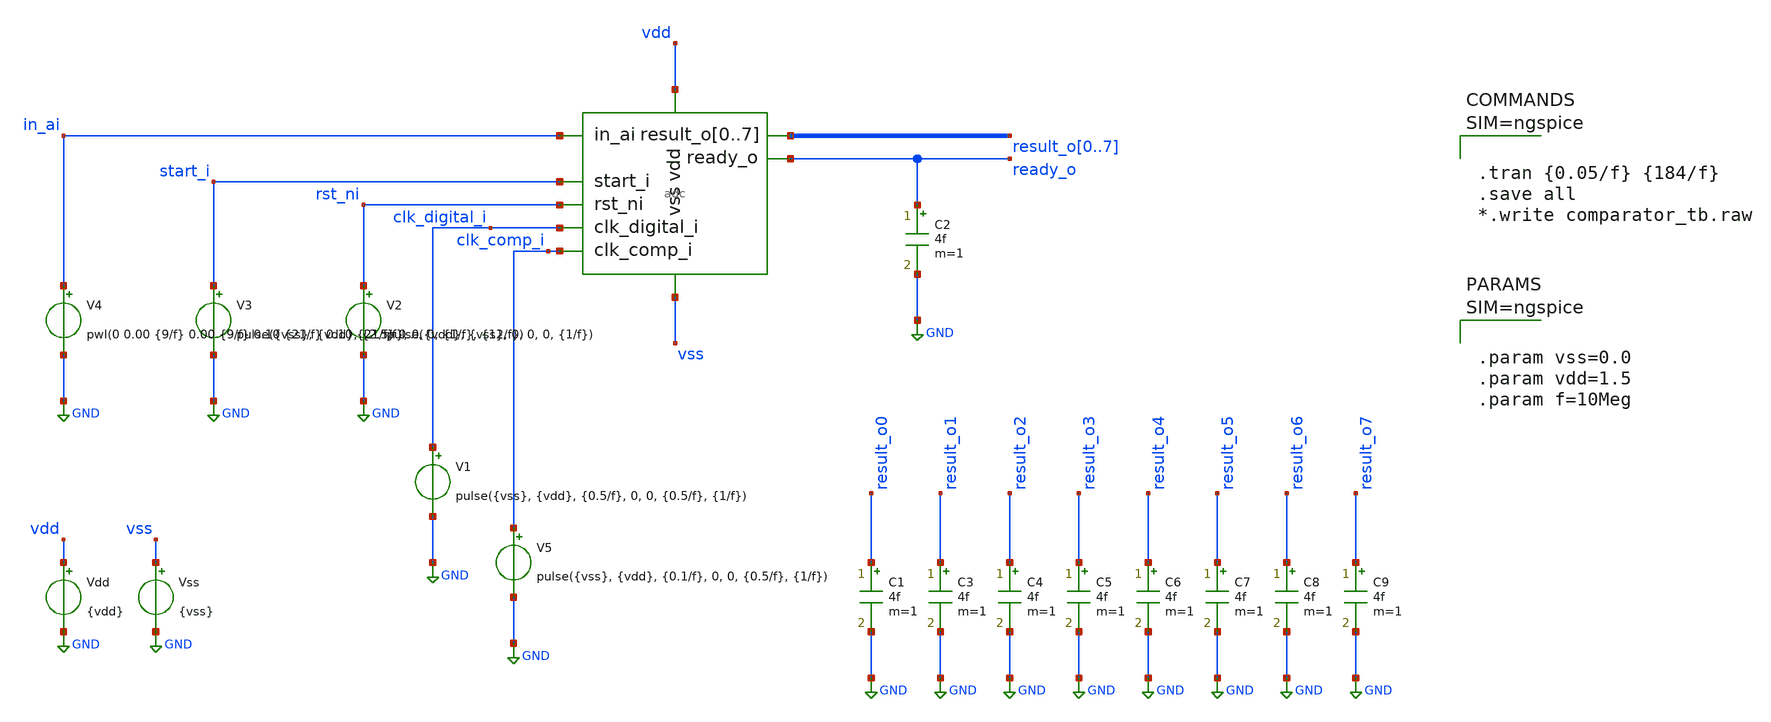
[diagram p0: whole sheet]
** sch_path: designs/basic1/adc_tb.sch
* IHP-GmbH/IHP-Open-PDK/ihp-sg13g2/libs.tech/xschem/sg13g2_stdcells/sg13g2_inv_2.sch:
* Copyright 2023 IHP PDK Authors
* Licensed under the Apache License, Version 2.0 (the "License");
**.subckt adc_tb
x1 in_ai start_i rst_ni clk_digital_i result_o0 result_o1 result_o2 result_o3 result_o4 result_o5
+ result_o6 result_o7 ready_o vdd vss clk_comp_i adc
V1 clk_digital_i GND pulse({vss}, {vdd}, {0.5/f}, 0, 0, {0.5/f}, {1/f})
V2 rst_ni GND pulse({vdd}, {vss}, 0, 0, 0, {1/f})
V3 start_i GND pulse({vss}, {vdd}, {2.5/f}, 0, 0, {1/f}, {12/f})
V4 in_ai GND pwl(0 0.00 {9/f} 0.00 {9/f} 0.10 {21/f} 0.10 {21/f} 0.20 {33/f} 0.20 {33/f} 0.30 {45/f}
+ 0.30 {45/f} 0.40 {57/f} 0.40 {57/f} 0.50 {69/f} 0.50 {69/f} 0.60 {81/f} 0.60 {81/f} 0.70 {93/f} 0.70
+ {93/f} 0.80 {105/f} 0.80 {105/f} 0.90 {117/f} 0.90 {117/f} 1.00 {129/f} 1.00 {129/f} 1.10 {141/f} 1.10
+ {141/f} 1.20 {153/f} 1.20 {153/f} 1.30 {165/f} 1.30 {165/f} 1.40 {177/f} 1.40)
.save i(v4)
Vdd vdd GND {vdd}
Vss vss GND {vss}
C1 result_o0 GND 4f m=1
C2 ready_o GND 4f m=1
C3 result_o1 GND 4f m=1
C4 result_o2 GND 4f m=1
C5 result_o3 GND 4f m=1
V5 clk_comp_i GND pulse({vss}, {vdd}, {0.1/f}, 0, 0, {0.5/f}, {1/f})
C6 result_o4 GND 4f m=1
C7 result_o5 GND 4f m=1
C8 result_o6 GND 4f m=1
C9 result_o7 GND 4f m=1
**** begin user architecture code

.lib $::SG13G2_MODELS/cornerMOSlv.lib mos_tt
.lib $::SG13G2_MODELS/cornerCAP.lib cap_typ
.include $::PDK_ROOT/ihp-sg13g2/libs.ref/sg13g2_stdcell/spice/sg13g2_stdcell.spice




.tran {0.05/f} {184/f}
.save all
*.write comparator_tb.raw






.param vss=0.0
.param vdd=1.5
.param f=10Meg






.model adc_buff_clk adc_bridge(in_low = 'vdd/2' in_high = 'vdd/2')

.control
pre_set auto_bridge_d_out =  ( ".model auto_bridge_out bidi_bridge(direction=0 out_high=1.5
+ t_rise=0.1n t_fall=0.1n)"    "auto_bridge_out%d [ %s ] [ %s ] null auto_bridge_out" )
pre_set auto_bridge_d_in =  ( ".model auto_bridge_in bidi_bridge(direction=1 in_low=0.5 in_high=1)"
+    "auto_bridge_in%d [ %s ] [ %s ] null auto_bridge_in" )
.endc



**** end user architecture code
**.ends

* expanding   symbol:  adc.sym # of pins=9
** sym_path: designs/basic1/adc.sym
** sch_path: designs/basic1/adc.sch
.subckt adc in_ai start_i rst_ni clk_digital_i result_o0 result_o1 result_o2 result_o3 result_o4
+ result_o5 result_o6 result_o7 ready_o vdd vss clk_comp_i
*.ipin in_ai
*.ipin clk_digital_i
*.ipin vss
*.ipin vdd
*.ipin rst_ni
*.ipin start_i
*.opin ready_o
*.opin result_o0,result_o1,result_o2,result_o3,result_o4,result_o5,result_o6,result_o7
*.ipin clk_comp_i
x3 sample dac_o0 dac_o1 dac_o2 dac_o3 dac_o4 dac_o5 dac_o6 dac_o7 vss vdd cdac
A2 [ clk_digital_i ] [ net1 ] adc_buff_clk
A1 [ net1 start_i rst_ni comp_real ] [ ready_o sample_o dac_o0 dac_o1 dac_o2 dac_o3 dac_o4 dac_o5
+ dac_o6 dac_o7 result_o0 result_o1 result_o2 result_o3 result_o4 result_o5 result_o6 result_o7 ] adc
A3 [ %vd(sample vdd) ] [ comp ] comp
A4 [ comp ] [ comp_a ] dac_buff
* noconn %vd(sample vdd)
x2 clk_comp_i sample vdd comp_real_neg comp_real_pos vss vdd clk_comp_ni comparator
x4 clk_comp_ni clk_comp_i VDD VSS sg13g2_inv_1
x5 comp_real comp_real_pos comp_real_neg VDD VSS sg13g2_nand2b_1
.ends


* expanding   symbol:  /workspaces/ngspice_cosim_inv/designs/cdac/cdac.sym # of pins=4
** sym_path: designs/cdac/cdac.sym
** sch_path: designs/cdac/cdac.sch
.subckt cdac VIN CTRL0 CTRL1 CTRL2 CTRL3 CTRL4 CTRL5 CTRL6 CTRL7 VSS VDD
*.ipin VIN
*.ipin CTRL0,CTRL1,CTRL2,CTRL3,CTRL4,CTRL5,CTRL6,CTRL7
*.ipin VSS
*.ipin VDD
XC2 VIN l1 cap_cmim w=7.297e-5 l=7.298e-5 m=1 mm_ok=1
XC3 VIN l2 cap_cmim w=5.158e-5 l=5.159e-5 m=1 mm_ok=1
XC4 VIN l3 cap_cmim w=3.646e-5 l=3.646e-5 m=1 mm_ok=1
XC5 VIN VSS cap_cmim w=6.402e-6 l=6.402e-6 m=1 mm_ok=1
x1 l1 CTRL0 VDD VSS sg13g2_inv_2
x2 l2 CTRL1 VDD VSS sg13g2_inv_2
x3 l3 CTRL2 VDD VSS sg13g2_inv_2
x4 l4 CTRL3 VDD VSS sg13g2_inv_2
XC6 VIN l4 cap_cmim w=2.577e-5 l=2.577e-5 m=1 mm_ok=1
XC7 VIN l5 cap_cmim w=1.820e-5 l=1.820e-5 m=1 mm_ok=1
XC8 VIN l6 cap_cmim w=1.286e-5 l=1.286e-5 m=1 mm_ok=1
XC9 VIN l7 cap_cmim w=9.077e-6 l=9.077e-6 m=1 mm_ok=1
x5 l5 CTRL4 VDD VSS sg13g2_inv_2
x6 l6 CTRL5 VDD VSS sg13g2_inv_2
x7 l7 CTRL6 VDD VSS sg13g2_inv_2
x8 l8 CTRL7 VDD VSS sg13g2_inv_2
XC1 VIN l8 cap_cmim w=6.402e-6 l=6.402e-6 m=1 mm_ok=1
.ends


* expanding   symbol:  /workspaces/ngspice_cosim_inv/designs/comparator_dt/comparator.sym # of
*+ pins=8
** sym_path: designs/comparator_dt/comparator.sym
** sch_path: designs/comparator_dt/comparator.sch
.subckt comparator clk_i pos_ai neg_ai neg_o pos_o VSS VDD clk_ni
*.ipin pos_ai
*.ipin neg_ai
*.ipin VSS
*.ipin VDD
*.opin neg_o
*.opin pos_o
*.ipin clk_i
*.ipin clk_ni
XM12 neg_buf clk_i VDD VDD sg13_lv_pmos w=1.0u l=0.13u ng=1 m=1 mm_ok=1
XM13 pos_buf clk_i VDD VDD sg13_lv_pmos w=1.0u l=0.13u ng=1 m=1 mm_ok=1
XM14 net1 pos_ai neg_buf VSS sg13_lv_nmos w=1.0u l=0.13u ng=1 m=1 mm_ok=1
XM15 net1 neg_ai pos_buf VSS sg13_lv_nmos w=1.0u l=0.13u ng=1 m=1 mm_ok=1
XM16 VSS clk_i net1 VSS sg13_lv_nmos w=1.0u l=0.13u ng=1 m=1 mm_ok=1
XM17 net2 clk_ni VDD VDD sg13_lv_pmos w=2.0u l=0.13u ng=2 m=1 mm_ok=1
XM18 pos_o neg_o net2 VDD sg13_lv_pmos w=2.0u l=0.13u ng=2 m=1 mm_ok=1
XM19 neg_o pos_o net2 VDD sg13_lv_pmos w=2.0u l=0.13u ng=2 m=1 mm_ok=1
XM20 VSS neg_buf pos_o VSS sg13_lv_nmos w=1.0u l=0.13u ng=1 m=1 mm_ok=1
XM21 VSS neg_o pos_o VSS sg13_lv_nmos w=1.0u l=0.13u ng=1 m=1 mm_ok=1
XM22 VSS pos_o neg_o VSS sg13_lv_nmos w=1.0u l=0.13u ng=1 m=1 mm_ok=1
XM23 VSS pos_buf neg_o VSS sg13_lv_nmos w=1.0u l=0.13u ng=1 m=1 mm_ok=1
XC1 neg_buf VSS cap_cmim w=1.41e-5 l=1.41e-5 m=1 mm_ok=1
XC2 pos_buf VSS cap_cmim w=1.41e-5 l=1.41e-5 m=1 mm_ok=1
.ends


* expanding   symbol:  sg13g2_stdcells/sg13g2_inv_1.sym # of pins=2
** sym_path: sg13g2_stdcells/sg13g2_inv_1.sym
** sch_path: sg13g2_stdcells/sg13g2_inv_1.sch
.subckt sg13g2_inv_1 Y A VDD VSS
*.opin Y
*.ipin A
*.iopin VDD
*.iopin VSS
XM1 Y A VSS VSS sg13_lv_nmos w=740.00n l=130.00n ng=1 m=1 mm_ok=1
XM2 Y A VDD VDD sg13_lv_pmos w=1.12u l=130.00n ng=1 m=1 mm_ok=1
.ends


* expanding   symbol:  sg13g2_stdcells/sg13g2_nand2b_1.sym # of pins=3
** sym_path: sg13g2_stdcells/sg13g2_nand2b_1.sym
** sch_path: sg13g2_stdcells/sg13g2_nand2b_1.sch
.subckt sg13g2_nand2b_1 Y A_N B VDD VSS
*.opin Y
*.ipin B
*.ipin A_N
*.iopin VDD
*.iopin VSS
XM1 net1 A_N VSS VSS sg13_lv_nmos w=550.00n l=130.00n ng=1 m=1 mm_ok=1
XM2 Y net1 net2 VSS sg13_lv_nmos w=740.00n l=130.00n ng=1 m=1 mm_ok=1
XM3 net2 B VSS VSS sg13_lv_nmos w=740.00n l=130.00n ng=1 m=1 mm_ok=1
XM4 Y B VDD VDD sg13_lv_pmos w=1.12u l=130.00n ng=1 m=1 mm_ok=1
XM5 net1 A_N VDD VDD sg13_lv_pmos w=840.00n l=130.00n ng=1 m=1 mm_ok=1
XM6 Y net1 VDD VDD sg13_lv_pmos w=1.12u l=130.00n ng=1 m=1 mm_ok=1
.ends


* expanding   symbol:  sg13g2_stdcells/sg13g2_inv_2.sym # of pins=2
** sym_path: sg13g2_stdcells/sg13g2_inv_2.sym
** sch_path: sg13g2_stdcells/sg13g2_inv_2.sch
.subckt sg13g2_inv_2 Y A VDD VSS
*.opin Y
*.ipin A
*.iopin VDD
*.iopin VSS
XM1 Y A VSS VSS sg13_lv_nmos w=1.48u l=130.00n ng=2 m=1 mm_ok=1
XM2 Y A VDD VDD sg13_lv_pmos w=2.24u l=130.00n ng=2 m=1 mm_ok=1
.ends

.GLOBAL GND
**** begin user architecture code
.model adc d_cosim simulation="ivlng" sim_args=["adc"]
.model dac_buff dac_bridge input_load=1e-15 t_rise=0.1n t_fall=0.1n  out_low=0 out_high=1.5
.model comp adc_bridge in_low=0 in_high=0
**** end user architecture code
.end
